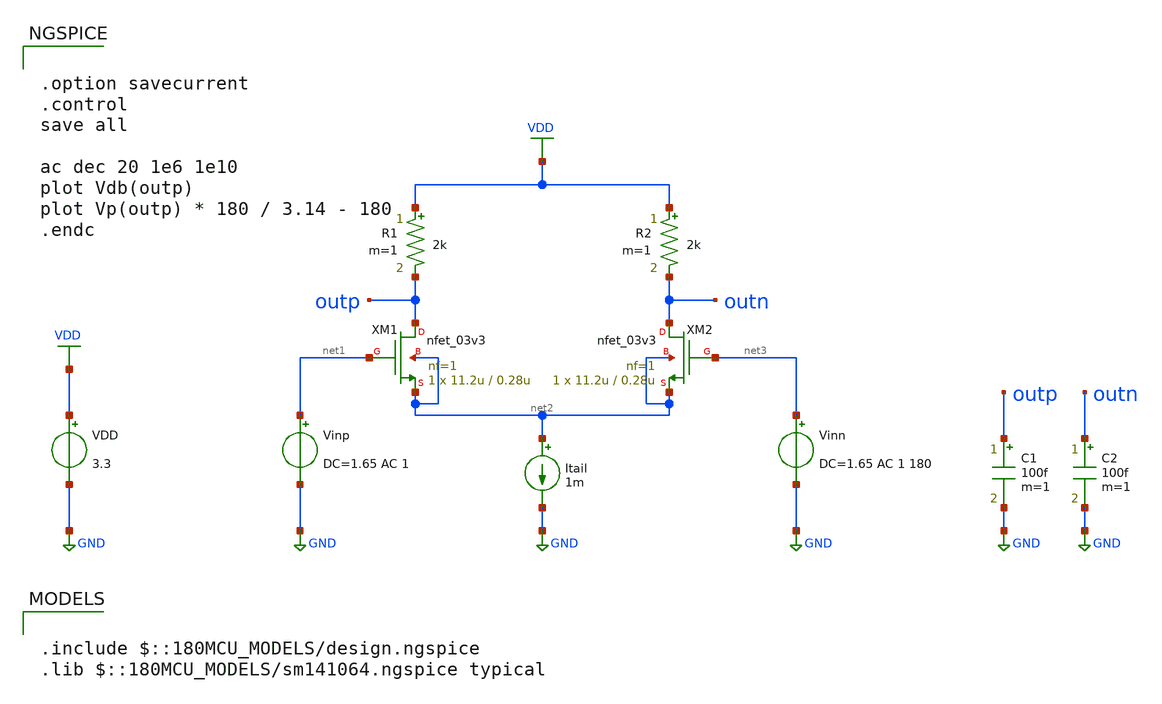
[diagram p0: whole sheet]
** sch_path: fifty_nifty/08_diff_ac.sch
**.subckt 08_diff_ac
XM1 outp net1 net2 net2 nfet_03v3 L=0.28u W=11.2u nf=1 ad='int((nf+1)/2) * W/nf * 0.18u' as='int((nf+2)/2) * W/nf * 0.18u'
+ pd='2*int((nf+1)/2) * (W/nf + 0.18u)' ps='2*int((nf+2)/2) * (W/nf + 0.18u)' nrd='0.18u / W' nrs='0.18u / W'
+ sa=0 sb=0 sd=0 m=1
VDD VDD GND 3.3
XM2 outn net3 net2 net2 nfet_03v3 L=0.28u W=11.2u nf=1 ad='int((nf+1)/2) * W/nf * 0.18u' as='int((nf+2)/2) * W/nf * 0.18u'
+ pd='2*int((nf+1)/2) * (W/nf + 0.18u)' ps='2*int((nf+2)/2) * (W/nf + 0.18u)' nrd='0.18u / W' nrs='0.18u / W'
+ sa=0 sb=0 sd=0 m=1
Itail net2 GND 1m
Vinp net1 GND DC=1.65 AC 1
R1 VDD outp 2k m=1
R2 VDD outn 2k m=1
Vinn net3 GND DC=1.65 AC 1 180
C1 outp GND 100f m=1
C2 outn GND 100f m=1
**** begin user architecture code

.option savecurrent
.control
save all

ac dec 20 1e6 1e10
plot Vdb(outp)
plot Vp(outp) * 180 / 3.14 - 180
.endc


.include $::180MCU_MODELS/design.ngspice
.lib $::180MCU_MODELS/sm141064.ngspice typical

**** end user architecture code
**.ends
.GLOBAL GND
.GLOBAL VDD
.end
